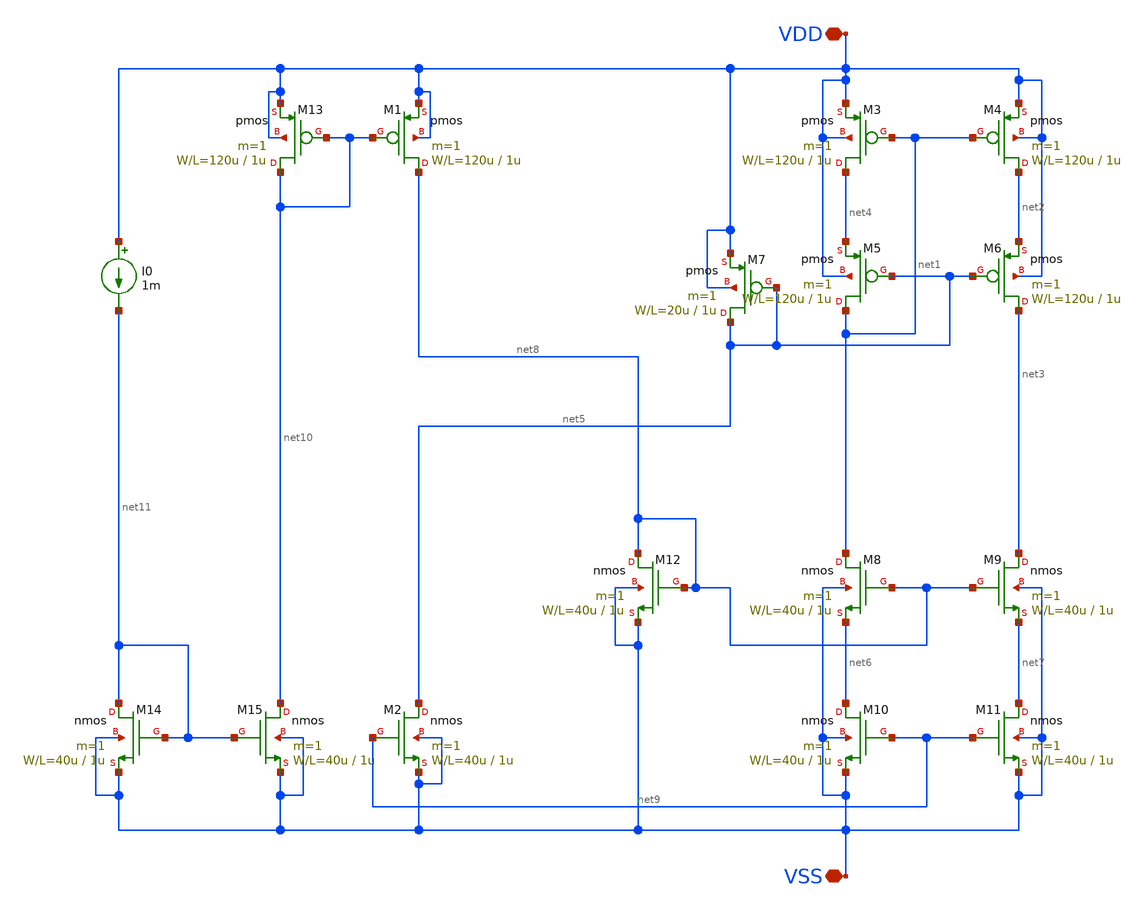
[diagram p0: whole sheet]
** sch_path: OR1/PTC06/opamp/rail2rail.sch
**.subckt rail2rail VDD VSS
*.iopin VDD
*.iopin VSS
M1 net8 net10 VDD VDD pmos L=1u W=120u m=1
M3 net4 net1 VDD VDD pmos L=1u W=120u m=1
M4 net2 net1 VDD VDD pmos L=1u W=120u m=1
M5 net1 net5 net4 VDD pmos L=1u W=120u m=1
M6 net3 net5 net2 VDD pmos L=1u W=120u m=1
M7 net5 net5 VDD VDD pmos L=1u W=20u m=1
M8 net1 net8 net6 VSS nmos L=1u W=40u m=1
M9 net3 net8 net7 VSS nmos L=1u W=40u m=1
M10 net6 net9 VSS VSS nmos L=1u W=40u m=1
M11 net7 net9 VSS VSS nmos L=1u W=40u m=1
M12 net8 net8 VSS VSS nmos L=1u W=40u m=1
M2 net5 net9 VSS VSS nmos L=1u W=40u m=1
M13 net10 net10 VDD VDD pmos L=1u W=120u m=1
M14 net11 net11 VSS VSS nmos L=1u W=40u m=1
M15 net10 net11 VSS VSS nmos L=1u W=40u m=1
I0 VDD net11 1m
**.ends
.end
